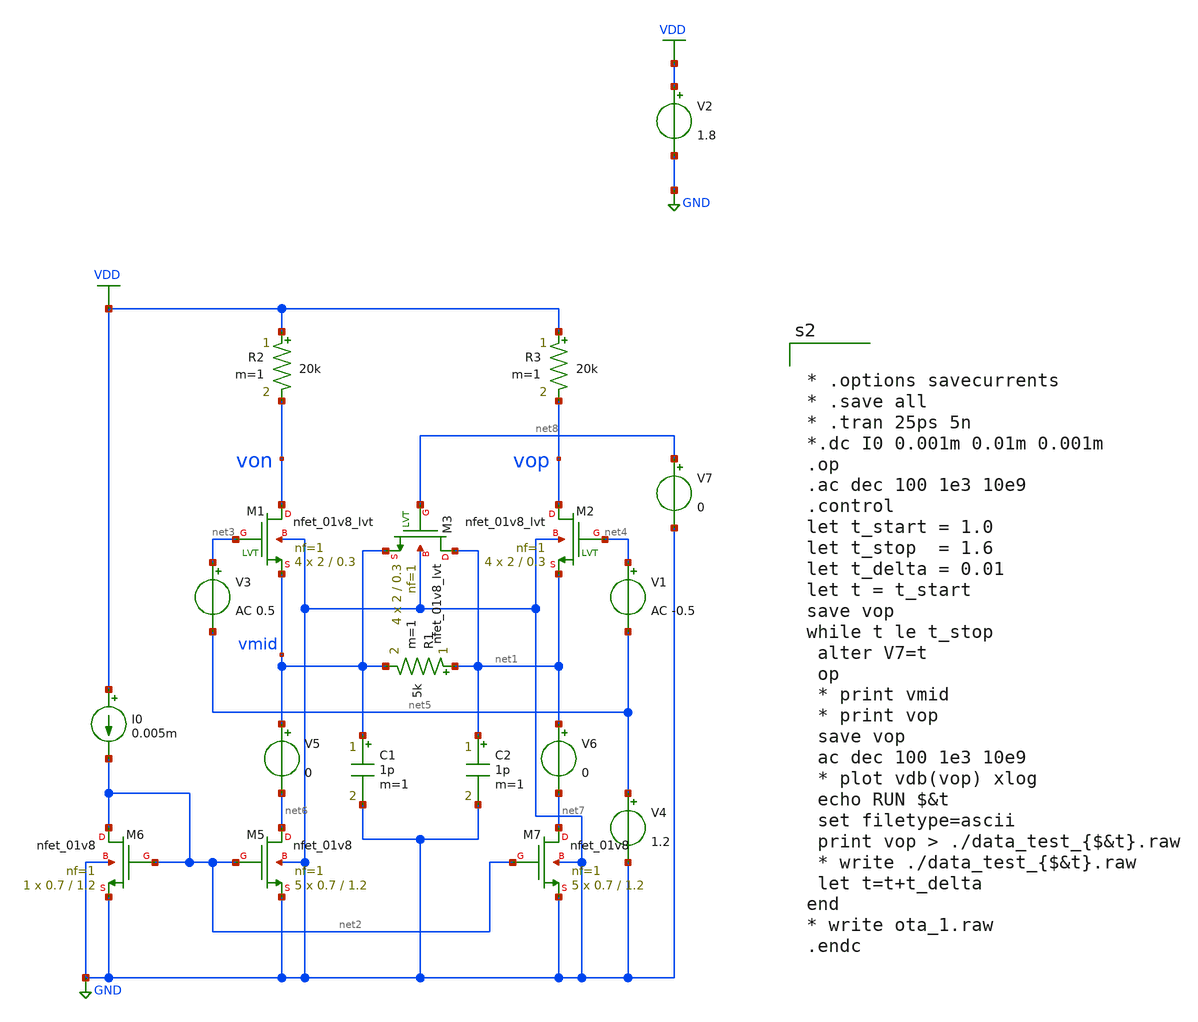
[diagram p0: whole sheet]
** sch_path: xschem/ota_wideband.sch
**.subckt ota_wideband
V2 VDD GND 1.8
XM1 von net3 vmid GND sky130_fd_pr__nfet_01v8_lvt L=0.3 W=2 nf=1 ad='int((nf+1)/2) * W/nf * 0.29' as='int((nf+2)/2) * W/nf * 0.29'
+ pd='2*int((nf+1)/2) * (W/nf + 0.29)' ps='2*int((nf+2)/2) * (W/nf + 0.29)' nrd='0.29 / W' nrs='0.29 / W'
+ sa=0 sb=0 sd=0 mult=4 m=4
XM2 vop net4 net1 GND sky130_fd_pr__nfet_01v8_lvt L=0.3 W=2 nf=1 ad='int((nf+1)/2) * W/nf * 0.29' as='int((nf+2)/2) * W/nf * 0.29'
+ pd='2*int((nf+1)/2) * (W/nf + 0.29)' ps='2*int((nf+2)/2) * (W/nf + 0.29)' nrd='0.29 / W' nrs='0.29 / W'
+ sa=0 sb=0 sd=0 mult=4 m=4
XM5 net6 net2 GND GND sky130_fd_pr__nfet_01v8 L=1.2 W=0.7 nf=1 ad='int((nf+1)/2) * W/nf * 0.29' as='int((nf+2)/2) * W/nf * 0.29'
+ pd='2*int((nf+1)/2) * (W/nf + 0.29)' ps='2*int((nf+2)/2) * (W/nf + 0.29)' nrd='0.29 / W' nrs='0.29 / W'
+ sa=0 sb=0 sd=0 mult=5 m=5
XM6 net2 net2 GND GND sky130_fd_pr__nfet_01v8 L=1.2 W=0.7 nf=1 ad='int((nf+1)/2) * W/nf * 0.29' as='int((nf+2)/2) * W/nf * 0.29'
+ pd='2*int((nf+1)/2) * (W/nf + 0.29)' ps='2*int((nf+2)/2) * (W/nf + 0.29)' nrd='0.29 / W' nrs='0.29 / W'
+ sa=0 sb=0 sd=0 mult=1 m=1
I0 VDD net2 0.005m
V3 net3 net5 AC 0.5
V4 net5 GND 1.2
V5 vmid net6 0
V1 net4 net5 AC -0.5
XM7 net7 net2 GND GND sky130_fd_pr__nfet_01v8 L=1.2 W=0.7 nf=1 ad='int((nf+1)/2) * W/nf * 0.29' as='int((nf+2)/2) * W/nf * 0.29'
+ pd='2*int((nf+1)/2) * (W/nf + 0.29)' ps='2*int((nf+2)/2) * (W/nf + 0.29)' nrd='0.29 / W' nrs='0.29 / W'
+ sa=0 sb=0 sd=0 mult=5 m=5
V6 net1 net7 0
R1 net1 vmid 5k m=1
R2 VDD von 20k m=1
R3 VDD vop 20k m=1
C1 vmid GND 1p m=1
C2 net1 GND 1p m=1
XM3 net1 net8 vmid GND sky130_fd_pr__nfet_01v8_lvt L=0.3 W=2 nf=1 ad='int((nf+1)/2) * W/nf * 0.29' as='int((nf+2)/2) * W/nf * 0.29'
+ pd='2*int((nf+1)/2) * (W/nf + 0.29)' ps='2*int((nf+2)/2) * (W/nf + 0.29)' nrd='0.29 / W' nrs='0.29 / W'
+ sa=0 sb=0 sd=0 mult=4 m=4
V7 net8 GND 0
**** begin user architecture code
.lib $::SKYWATER_MODELS/sky130.lib.spice tt
* .include $::PDKPATH/libs.ref/sky130_fd_sc_hvl/spice/sky130_fd_sc_hvl.spice



* .options savecurrents
* .save all
* .tran 25ps 5n
*.dc I0 0.001m 0.01m 0.001m
.op
.ac dec 100 1e3 10e9
.control
let t_start = 1.0
let t_stop  = 1.6
let t_delta = 0.01
let t = t_start
save vop
while t le t_stop
 alter V7=t
 op
 * print vmid
 * print vop
 save vop
 ac dec 100 1e3 10e9
 * plot vdb(vop) xlog
 echo RUN $&t
 set filetype=ascii
 print vop > ./data_test_{$&t}.raw
 * write ./data_test_{$&t}.raw
 let t=t+t_delta
end
* write ota_1.raw
.endc


**** end user architecture code
**.ends
.GLOBAL VDD
.GLOBAL GND
.end
